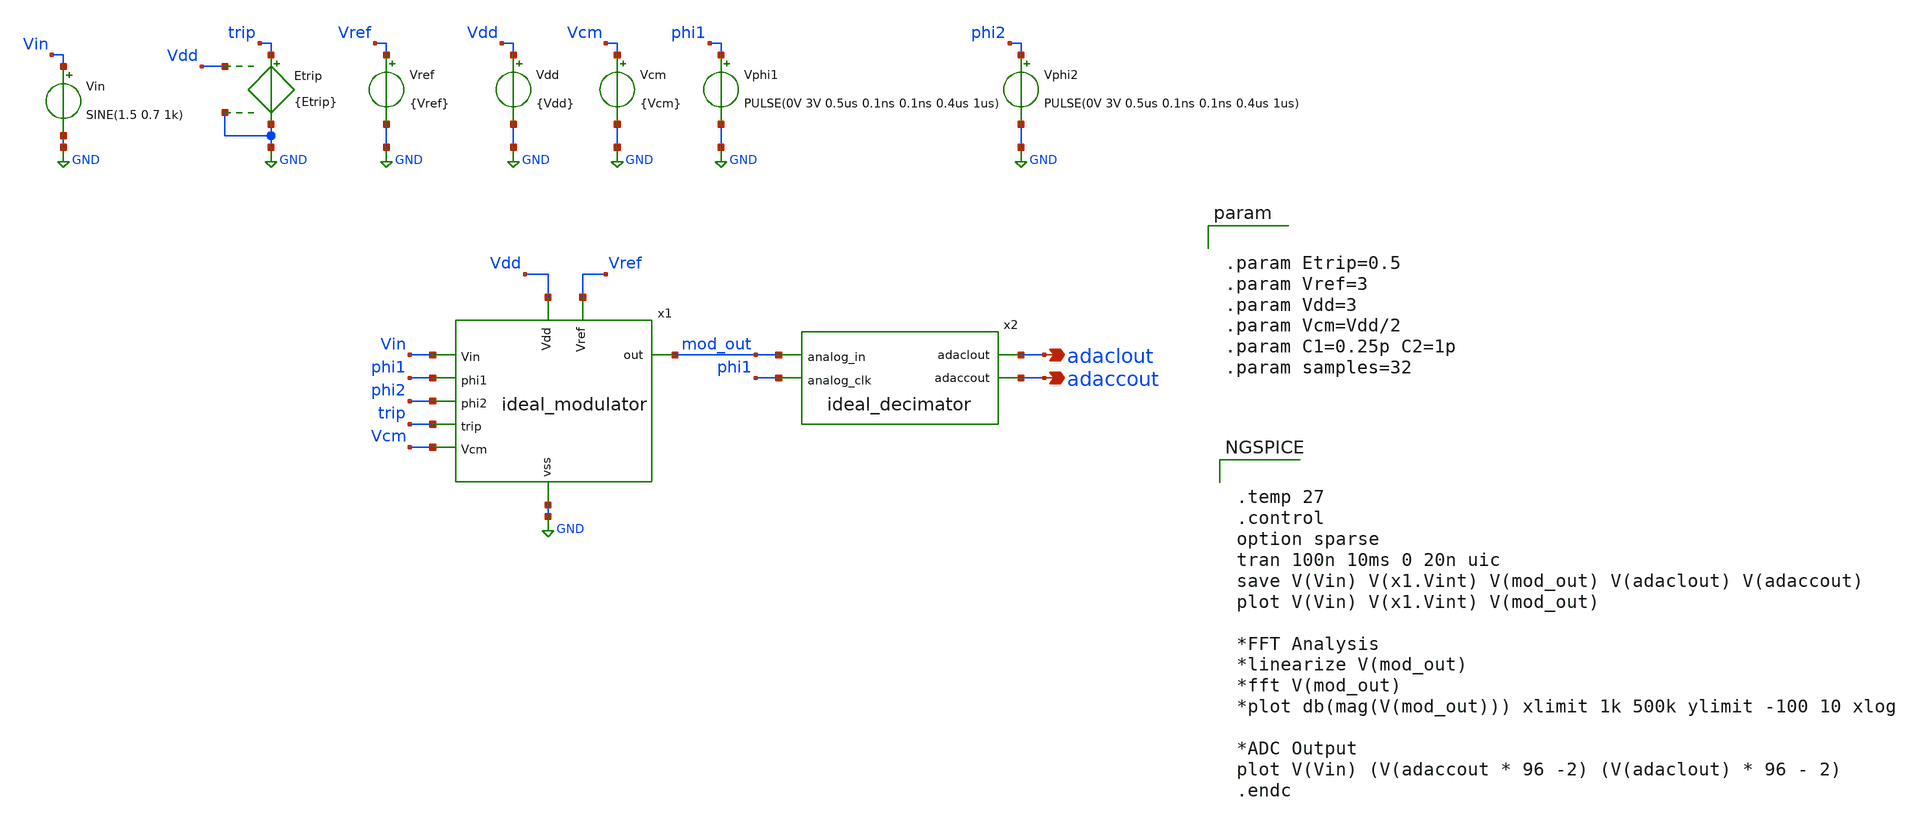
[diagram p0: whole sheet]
** sch_path: 2_ideal_circuits/first_order_delta_sigma_adc_single_ended.sch
**.subckt first_order_delta_sigma_adc_single_ended adaclout adaccout
*.opin adaclout
*.opin adaccout
Vin Vin GND SINE(1.5 0.7 1k)
Vref Vref GND {Vref}
Vdd Vdd GND {Vdd}
Vcm Vcm GND {Vcm}
Vphi1 phi1 GND PULSE(0V 3V 0.5us 0.1ns 0.1ns 0.4us 1us)
Vphi2 phi2 GND PULSE(0V 3V 0.5us 0.1ns 0.1ns 0.4us 1us)
Etrip trip GND Vdd GND {Etrip}
x1 Vdd Vin mod_out phi1 phi2 trip Vref Vcm GND ideal_modulator
x2 mod_out phi1 adaclout adaccout ideal_decimator samples={samples}
**** begin user architecture code


.param Etrip=0.5
.param Vref=3
.param Vdd=3
.param Vcm=Vdd/2
.param C1=0.25p C2=1p
.param samples=32




.temp 27
.control
option sparse
tran 100n 10ms 0 20n uic
save V(Vin) V(x1.Vint) V(mod_out) V(adaclout) V(adaccout)
plot V(Vin) V(x1.Vint) V(mod_out)

*FFT Analysis
*linearize V(mod_out)
*fft V(mod_out)
*plot db(mag(V(mod_out))) xlimit 1k 500k ylimit -100 10 xlog

*ADC Output
plot V(Vin) (V(adaccout * 96 -2) (V(adaclout) * 96 - 2)
.endc


**** end user architecture code
**.ends

* expanding   symbol:  ideal_modulator.sym # of pins=9
** sym_path: 2_ideal_circuits/ideal_modulator.sym
** sch_path: 2_ideal_circuits/ideal_modulator.sch
.subckt ideal_modulator Vdd Vin out phi1 phi2 trip Vref Vcm vss
*.opin out
*.ipin Vin
*.ipin phi1
*.ipin trip
*.ipin phi2
*.ipin Vcm
*.ipin Vref
*.ipin Vdd
*.iopin vss
S1 Vin net1 phi1 trip SW1
S2 net1 Vfb phi2 trip SW1
S3 diff net2 phi2 trip SW1
S4 net2 Vcm phi1 trip SW1
x1 Vcm diff Vint ideal_opamp
C2 diff Vint {C2} m=1
C1 net1 net2 {C1} m=1
x3 Vdd cmp Vint Vcm phi1 ideal_comparator
x5 Vfb cmp vss Vref ideal_inverter
x2 out cmp vss Vdd ideal_inverter
.ends


* expanding   symbol:  ideal_decimator.sym # of pins=4
** sym_path: 2_ideal_circuits/ideal_decimator.sym
.include /foss/designs/drms-elie3/2_ideal_circuits/ideal_decimator.cir

* expanding   symbol:  ideal_opamp.sym # of pins=3
** sym_path: ideal_opamp.sym
** sch_path: ideal_opamp.sch
.subckt ideal_opamp inp inn out
*.opin out
*.ipin inp
*.ipin inn
E1 out GND inp inn 1Meg
R1 out GND 100Meg m=1
.ends


* expanding   symbol:  ideal_comparator.sym # of pins=5
** sym_path: 2_ideal_circuits/ideal_comparator.sym
** sch_path: 2_ideal_circuits/ideal_comparator.sch
.subckt ideal_comparator Vdd Vout Vinn Vinp clk
*.ipin Vinp
*.ipin Vinn
*.opin Vout
*.iopin Vdd
*.iopin clk
E1 diff GND Vinp Vinn 1
S1 diff sample tp clk SW1
E2 net1 GND sample GND 1
C1 sample GND 100p m=1
S2 net1 hold clk tp SW1
C2 hold GND 100p m=1
B1 Vout GND V={v(hold)>0?v(Vdd):0}
Etp tp GND Vdd GND 0.5
**** begin user architecture code


.ic v(hold)=1 v(sample)=1


**** end user architecture code
.ends


* expanding   symbol:  ideal_inverter.sym # of pins=4
** sym_path: 2_ideal_circuits/ideal_inverter.sym
** sch_path: 2_ideal_circuits/ideal_inverter.sch
.subckt ideal_inverter out in vss vdd
*.iopin vdd
*.ipin in
*.opin out
*.iopin vss
B1 out GND V={v(in)>v(vdd)/2?v(vss):v(vdd)}
* noconn vdd
* noconn in
* noconn vss
.ends

.GLOBAL GND
**** begin user architecture code
.MODEL SW1 SW( VT=0.9 VH=0.01 RON=0.01 ROFF=10G )
**** end user architecture code
.end
